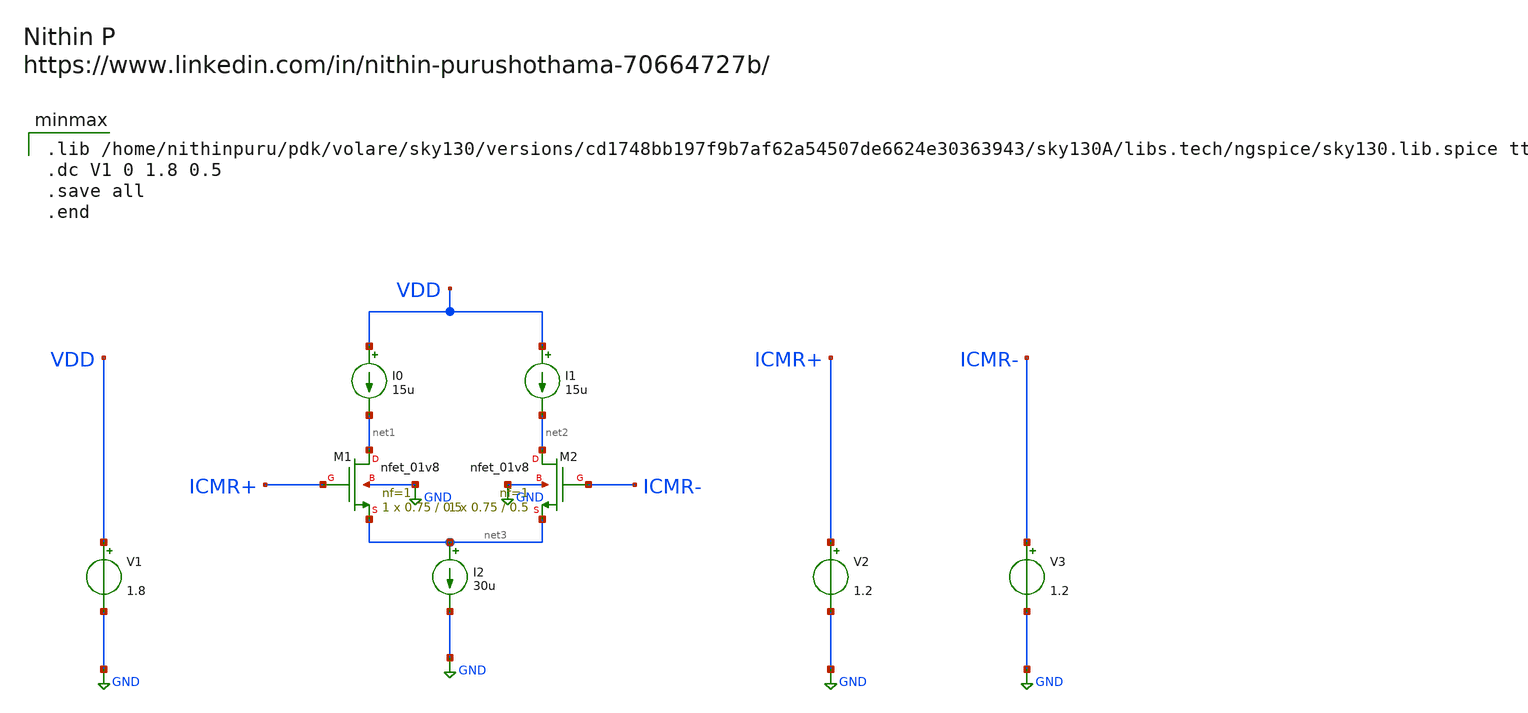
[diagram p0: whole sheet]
** sch_path: Schematics/NMOS Vth Calculation/minmaxNMOS.sch
**.subckt minmaxNMOS
V1 VDD GND 1.8
V2 ICMR+ GND 1.2
V3 ICMR- GND 1.2
XM1 net1 ICMR+ net3 GND sky130_fd_pr__nfet_01v8 L=0.5 W=0.75 nf=1 ad='int((nf+1)/2) * W/nf * 0.29' as='int((nf+2)/2) * W/nf * 0.29'
+ pd='2*int((nf+1)/2) * (W/nf + 0.29)' ps='2*int((nf+2)/2) * (W/nf + 0.29)' nrd='0.29 / W' nrs='0.29 / W'
+ sa=0 sb=0 sd=0 mult=1 m=1
XM2 net2 ICMR- net3 GND sky130_fd_pr__nfet_01v8 L=0.5 W=0.75 nf=1 ad='int((nf+1)/2) * W/nf * 0.29' as='int((nf+2)/2) * W/nf * 0.29'
+ pd='2*int((nf+1)/2) * (W/nf + 0.29)' ps='2*int((nf+2)/2) * (W/nf + 0.29)' nrd='0.29 / W' nrs='0.29 / W'
+ sa=0 sb=0 sd=0 mult=1 m=1
I0 VDD net1 15u
I1 VDD net2 15u
I2 net3 GND 30u
**** begin user architecture code

.lib /home/nithinpuru/pdk/volare/sky130/versions/cd1748bb197f9b7af62a54507de6624e30363943/sky130A/libs.tech/ngspice/sky130.lib.spice tt
.dc V1 0 1.8 0.5
.save all
.end

**** end user architecture code
**.ends
.GLOBAL GND
.end
